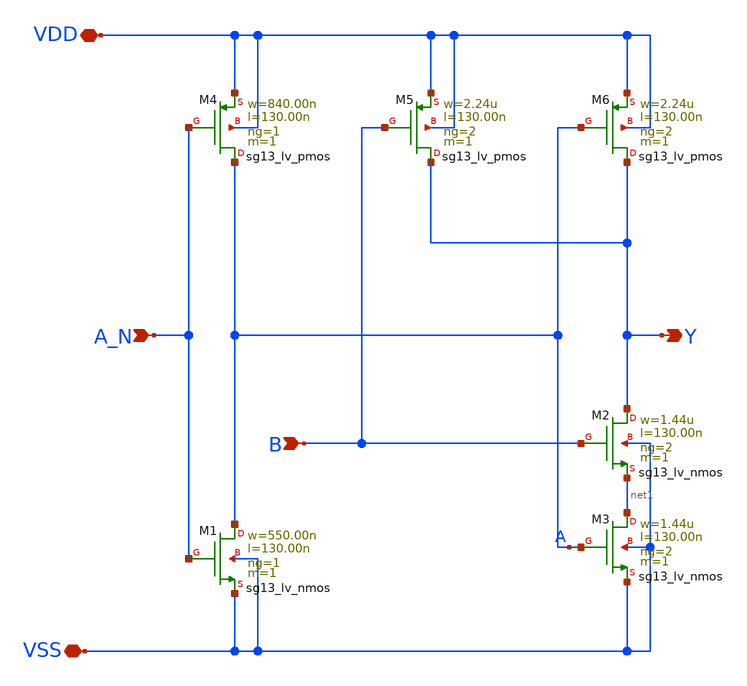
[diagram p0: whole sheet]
** sch_path: ihp-sg13g2/libs.tech/xschem/sg13g2_stdcells/sg13g2_nand2b_2.sch
* Copyright 2023 IHP PDK Authors
* Licensed under the Apache License, Version 2.0 (the "License");
* you may not use this file except in compliance with the License.
* You may obtain a copy of the License at
* https://www.apache.org/licenses/LICENSE-2.0
* Unless required by applicable law or agreed to in writing, software
* distributed under the License is distributed on an "AS IS" BASIS,
* WITHOUT WARRANTIES OR CONDITIONS OF ANY KIND, either express or implied.
* See the License for the specific language governing permissions and
* limitations under the License.
**.subckt sg13g2_nand2b_2 Y B A_N VDD VSS
*.opin Y
*.ipin B
*.ipin A_N
*.iopin VDD
*.iopin VSS
XM1 A A_N VSS VSS sg13_lv_nmos w=550.00n l=130.00n ng=1 m=1 mm_ok=1
XM2 Y B net1 VSS sg13_lv_nmos w=1.44u l=130.00n ng=2 m=1 mm_ok=1
XM3 net1 A VSS VSS sg13_lv_nmos w=1.44u l=130.00n ng=2 m=1 mm_ok=1
XM4 A A_N VDD VDD sg13_lv_pmos w=840.00n l=130.00n ng=1 m=1 mm_ok=1
XM5 Y B VDD VDD sg13_lv_pmos w=2.24u l=130.00n ng=2 m=1 mm_ok=1
XM6 Y A VDD VDD sg13_lv_pmos w=2.24u l=130.00n ng=2 m=1 mm_ok=1
**.ends
.end
